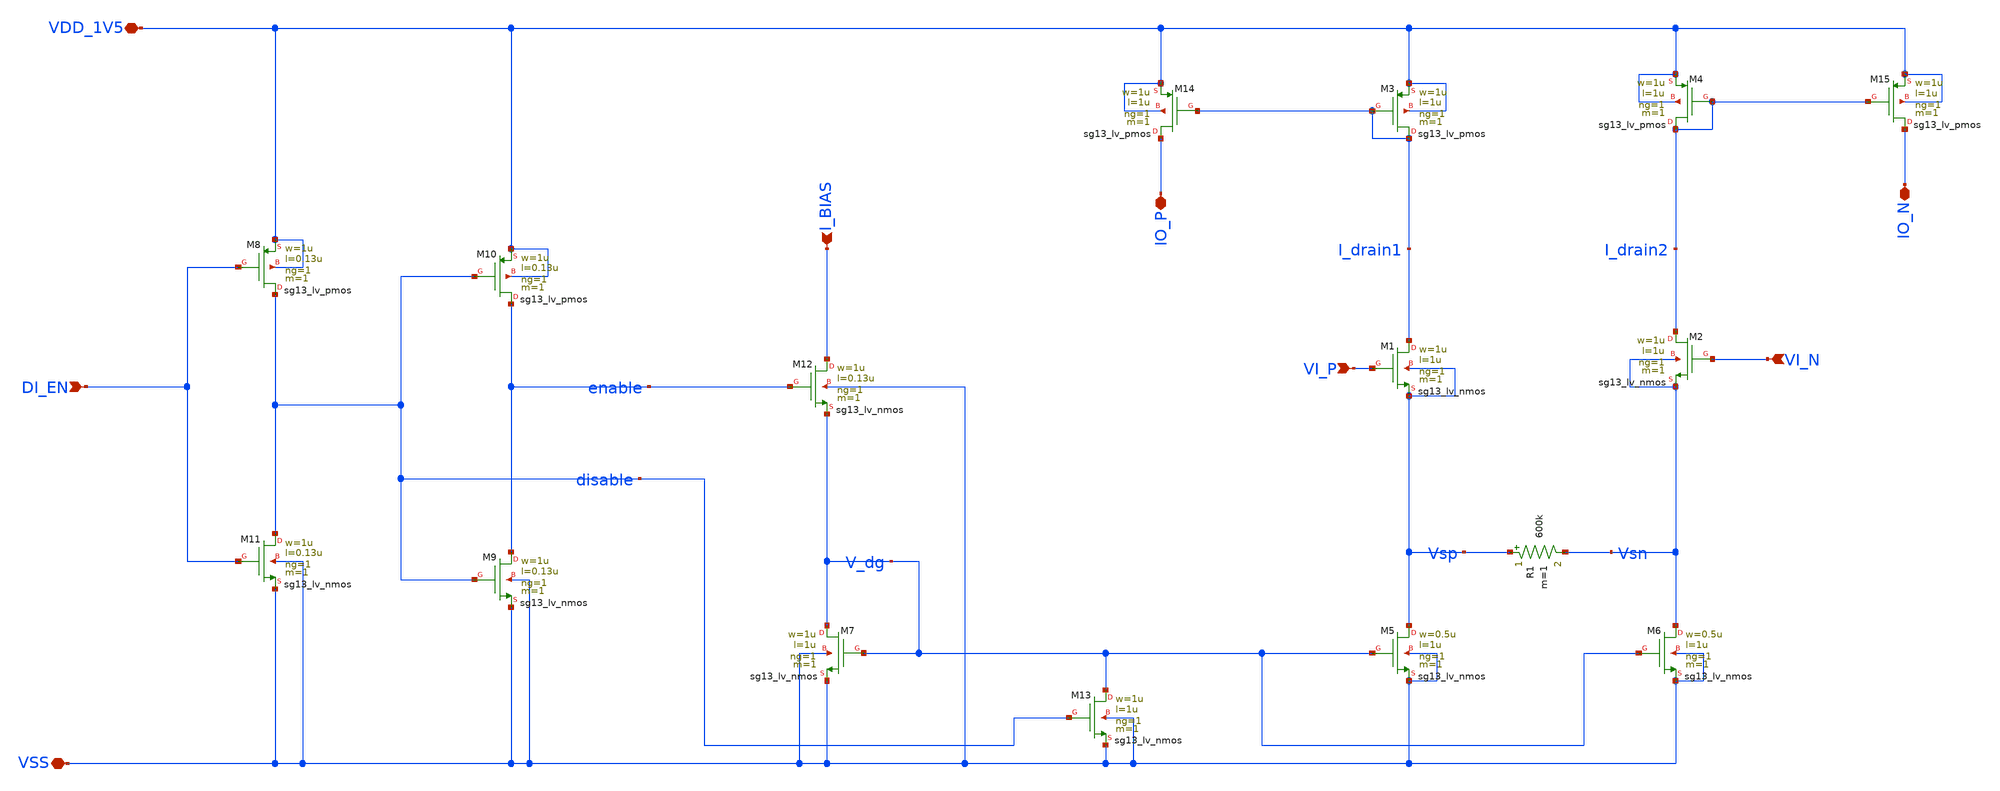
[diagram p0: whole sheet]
** sch_path: gm1.sch
**.subckt gm1 VI_N VI_P VSS VDD_1V5 IO_P IO_N I_BIAS DI_EN
*.ipin VI_N
*.ipin VI_P
*.iopin VSS
*.iopin VDD_1V5
*.iopin IO_P
*.iopin IO_N
*.ipin I_BIAS
*.ipin DI_EN
XM1 I_drain1 VI_P Vsp Vsp sg13_lv_nmos w=1u l=1u ng=1 m=1 mm_ok=1
XM2 I_drain2 VI_N Vsn Vsn sg13_lv_nmos w=1u l=1u ng=1 m=1 mm_ok=1
R1 Vsp Vsn 600k m=1
XM5 Vsp V_dg VSS VSS sg13_lv_nmos w=0.5u l=1u ng=1 m=1 mm_ok=1
XM6 Vsn V_dg VSS VSS sg13_lv_nmos w=0.5u l=1u ng=1 m=1 mm_ok=1
XM7 V_dg V_dg VSS VSS sg13_lv_nmos w=1u l=1u ng=1 m=1 mm_ok=1
XM8 disable DI_EN VDD_1V5 VDD_1V5 sg13_lv_pmos w=1u l=0.13u ng=1 m=1 mm_ok=1
XM9 enable disable VSS VSS sg13_lv_nmos w=1u l=0.13u ng=1 m=1 mm_ok=1
XM10 enable disable VDD_1V5 VDD_1V5 sg13_lv_pmos w=1u l=0.13u ng=1 m=1 mm_ok=1
XM11 disable DI_EN VSS VSS sg13_lv_nmos w=1u l=0.13u ng=1 m=1 mm_ok=1
XM12 I_BIAS enable V_dg VSS sg13_lv_nmos w=1u l=0.13u ng=1 m=1 mm_ok=1
XM3 I_drain1 I_drain1 VDD_1V5 VDD_1V5 sg13_lv_pmos w=1u l=1u ng=1 m=1 mm_ok=1
XM4 I_drain2 I_drain2 VDD_1V5 VDD_1V5 sg13_lv_pmos w=1u l=1u ng=1 m=1 mm_ok=1
XM14 IO_P I_drain1 VDD_1V5 VDD_1V5 sg13_lv_pmos w=1u l=1u ng=1 m=1 mm_ok=1
XM15 IO_N I_drain2 VDD_1V5 VDD_1V5 sg13_lv_pmos w=1u l=1u ng=1 m=1 mm_ok=1
XM13 V_dg disable VSS VSS sg13_lv_nmos w=1u l=1u ng=1 m=1 mm_ok=1
**.ends
.end
